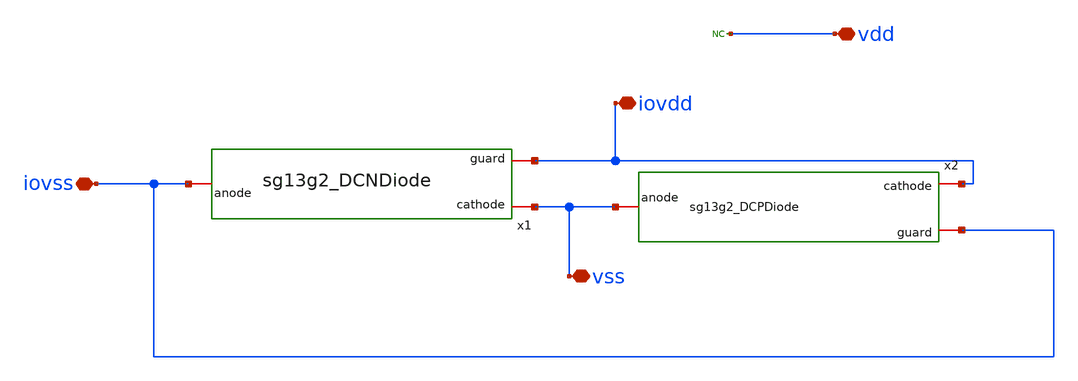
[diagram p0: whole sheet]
** sch_path: CDR4176-main/schematic/xschem/project_io/sg13g2_IOPadVSS/sg13g2_IOPadVSS.sch
**.subckt sg13g2_IOPadVSS iovss iovdd vss vdd
*.iopin iovss
*.iopin iovdd
*.iopin vss
*.iopin vdd
x1 vss iovss iovdd sg13g2_DCNDiode
x2 iovdd vss iovss sg13g2_DCPDiode
* noconn vdd
**.ends

* expanding   symbol:  project_io/sg13g2_DCNDiode/sg13g2_DCNDiode.sym # of pins=3
** sym_path: project_io/sg13g2_DCNDiode/sg13g2_DCNDiode.sym
** sch_path: project_io/sg13g2_DCNDiode/sg13g2_DCNDiode.sch
.subckt sg13g2_DCNDiode cathode anode guard
*.iopin cathode
*.iopin anode
*.iopin guard
XD1 anode cathode dantenna l=1.26u w=27.78u
XD2 anode cathode dantenna l=1.26u w=27.78u
.ends


* expanding   symbol:  project_io/sg13g2_DCPDiode/sg13g2_DCPDiode.sym # of pins=3
** sym_path: project_io/sg13g2_DCPDiode/sg13g2_DCPDiode.sym
** sch_path: project_io/sg13g2_DCPDiode/sg13g2_DCPDiode.sch
.subckt sg13g2_DCPDiode cathode anode guard
*.iopin cathode
*.iopin anode
*.iopin guard
XD1 anode cathode dpantenna l=1.26u w=27.78u
XD2 anode cathode dpantenna l=1.26u w=27.78u
.ends

.end
